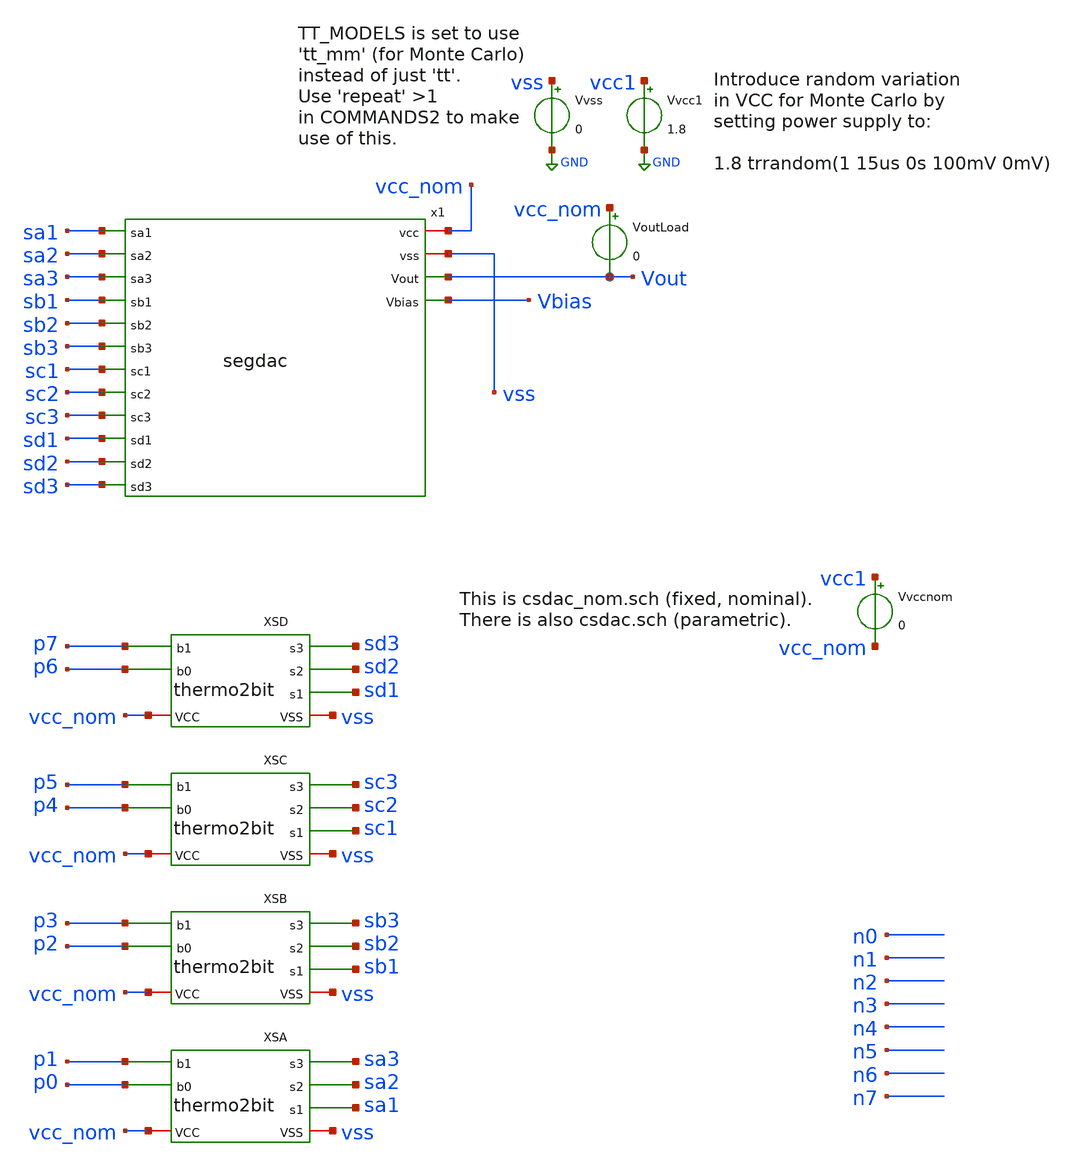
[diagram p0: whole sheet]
** sch_path: xschem/tb_segdac.sch
**.subckt tb_segdac
Vvcc1 vcc1 GND 1.8
Vvss vss GND 0
Vvccnom vcc1 vcc_nom 0
x1 sa1 vcc_nom sa2 vss sa3 Vout sb1 sb2 Vbias sb3 sc1 sc2 sc3 sd1 sd2 sd3 segdac
VoutLoad vcc_nom Vout 0
XSA vcc_nom vss sa3 p1 sa2 sa1 p0 thermo2bit
XSB vcc_nom vss sb3 p3 sb2 sb1 p2 thermo2bit
XSC vcc_nom vss sc3 p5 sc2 sc1 p4 thermo2bit
XSD vcc_nom vss sd3 p7 sd2 sd1 p6 thermo2bit
**** begin user architecture code




.param singlebits=0
.IF (singlebits == 1)
* Mode to just test each binary-weighted level:
Vxp0 p0 GND pulse 0v 1.8v 1u 1n 1n 1u 10u
Vxp1 p1 GND pulse 0v 1.8v 2u 1n 1n 1u 10u
Vxp2 p2 GND pulse 0v 1.8v 3u 1n 1n 1u 10u
Vxp3 p3 GND pulse 0v 1.8v 4u 1n 1n 1u 10u
Vxp4 p4 GND pulse 0v 1.8v 5u 1n 1n 1u 10u
Vxp5 p5 GND pulse 0v 1.8v 6u 1n 1n 1u 10u
Vxp6 p6 GND pulse 0v 1.8v 7u 1n 1n 1u 10u
Vxp7 p7 GND pulse 0v 1.8v 8u 1n 1n 1u 10u
Vxn0 n0 GND pulse 1.8v 0v 1u 1n 1n 1u 10u
Vxn1 n1 GND pulse 1.8v 0v 2u 1n 1n 1u 10u
Vxn2 n2 GND pulse 1.8v 0v 3u 1n 1n 1u 10u
Vxn3 n3 GND pulse 1.8v 0v 4u 1n 1n 1u 10u
Vxn4 n4 GND pulse 1.8v 0v 5u 1n 1n 1u 10u
Vxn5 n5 GND pulse 1.8v 0v 6u 1n 1n 1u 10u
Vxn6 n6 GND pulse 1.8v 0v 7u 1n 1n 1u 10u
Vxn7 n7 GND pulse 1.8v 0v 8u 1n 1n 1u 10u
.ELSEIF (singlebits == 0)
* Mode to test full 0..255 trange:
Vxp0 p0 GND pulse 1.8v 0v 0n 1n 1n 39n 80n
Vxp1 p1 GND pulse 1.8v 0v 0n 1n 1n 79n 160n
Vxp2 p2 GND pulse 1.8v 0v 0n 1n 1n 159n 320n
Vxp3 p3 GND pulse 1.8v 0v 0n 1n 1n 319n 640n
Vxp4 p4 GND pulse 1.8v 0v 0n 1n 1n 639n 1280n
Vxp5 p5 GND pulse 1.8v 0v 0n 1n 1n 1279n 2560n
Vxp6 p6 GND pulse 1.8v 0v 0n 1n 1n 2559n 5120n
Vxp7 p7 GND pulse 1.8v 0v 0n 1n 1n 5119n 10240n
Vxn0 n0 GND pulse 0v 1.8v 0n 1n 1n 39n 80n
Vxn1 n1 GND pulse 0v 1.8v 0n 1n 1n 79n 160n
Vxn2 n2 GND pulse 0v 1.8v 0n 1n 1n 159n 320n
Vxn3 n3 GND pulse 0v 1.8v 0n 1n 1n 319n 640n
Vxn4 n4 GND pulse 0v 1.8v 0n 1n 1n 639n 1280n
Vxn5 n5 GND pulse 0v 1.8v 0n 1n 1n 1279n 2560n
Vxn6 n6 GND pulse 0v 1.8v 0n 1n 1n 2559n 5120n
Vxn7 n7 GND pulse 0v 1.8v 0n 1n 1n 5119n 10240n
.ENDIF

.options savecurrents
.control

  * If using Monte Carlo, change to repeat to (say) 5:
  repeat 1
    save all
    tran 1n 12.8u
    write tb_segdac.raw i(vvss) vcc1 vbias vout i(vvccnom) i(voutload)
    + p0 p1 p2 p3 p4 p5 p6 p7
    + sa1 sa2 sa3 sb1 sb2 sb3 sc1 sc2 sc3 sd1 sd2 sd3
    set appendwrite
    reset
  end

*  save all
*  *reset
*  *alterparam MPW=4
*  *alterparam MMW=4
*  tran 1n 12.8u
*  write 11.raw i(vvcc) i(vvss) vpos vneg vbias

*  set appendwrite
*  alterparam MPW=4
*  alterparam MMW=4
*  reset
*  tran 1n 12.8u
*  write 11.raw i(vvcc) i(vvss) vpos vneg vbias

.endc




.lib $::SKYWATER_MODELS/sky130.lib.spice tt
.include $::SKYWATER_STDCELLS/sky130_fd_sc_hd.spice

**** end user architecture code
**.ends

* expanding   symbol:  segdac.sym # of pins=16
** sym_path: xschem/segdac.sym
** sch_path: xschem/segdac.sch
.subckt segdac sa1 vcc sa2 vss sa3 Vout sb1 sb2 Vbias sb3 sc1 sc2 sc3 sd1 sd2 sd3
*.iopin vcc
*.iopin vss
*.opin Vout
*.opin Vbias
*.ipin sa1
*.ipin sa2
*.ipin sa3
*.ipin sb1
*.ipin sb2
*.ipin sb3
*.ipin sc1
*.ipin sc2
*.ipin sc3
*.ipin sd1
*.ipin sd2
*.ipin sd3
XMprog Vbias vss vcc vcc sky130_fd_pr__pfet_01v8 L=0.6 W=0.5 nf=1 ad='int((nf+1)/2) * W/nf * 0.29' as='int((nf+2)/2) * W/nf * 0.29'
+ pd='2*int((nf+1)/2) * (W/nf + 0.29)' ps='2*int((nf+2)/2) * (W/nf + 0.29)' nrd='0.29 / W' nrs='0.29 / W'
+ sa=0 sb=0 sd=0 mult=1 m=1
XMmirror Vbias Vbias vss vss sky130_fd_pr__nfet_01v8 L=0.15 W=1 nf=1 ad='int((nf+1)/2) * W/nf * 0.29'
+ as='int((nf+2)/2) * W/nf * 0.29' pd='2*int((nf+1)/2) * (W/nf + 0.29)' ps='2*int((nf+2)/2) * (W/nf + 0.29)'
+ nrd='0.29 / W' nrs='0.29 / W' sa=0 sb=0 sd=0 mult=1 m=1
XMia1 net1 Vbias vss vss sky130_fd_pr__nfet_01v8 L=2.4 W=0.5 nf=1 ad='int((nf+1)/2) * W/nf * 0.29' as='int((nf+2)/2) * W/nf * 0.29'
+ pd='2*int((nf+1)/2) * (W/nf + 0.29)' ps='2*int((nf+2)/2) * (W/nf + 0.29)' nrd='0.29 / W' nrs='0.29 / W'
+ sa=0 sb=0 sd=0 mult=1 m=1
XMia2 net2 Vbias vss vss sky130_fd_pr__nfet_01v8 L=2.4 W=0.5 nf=1 ad='int((nf+1)/2) * W/nf * 0.29' as='int((nf+2)/2) * W/nf * 0.29'
+ pd='2*int((nf+1)/2) * (W/nf + 0.29)' ps='2*int((nf+2)/2) * (W/nf + 0.29)' nrd='0.29 / W' nrs='0.29 / W'
+ sa=0 sb=0 sd=0 mult=1 m=1
XMia3 net3 Vbias vss vss sky130_fd_pr__nfet_01v8 L=2.4 W=0.5 nf=1 ad='int((nf+1)/2) * W/nf * 0.29' as='int((nf+2)/2) * W/nf * 0.29'
+ pd='2*int((nf+1)/2) * (W/nf + 0.29)' ps='2*int((nf+2)/2) * (W/nf + 0.29)' nrd='0.29 / W' nrs='0.29 / W'
+ sa=0 sb=0 sd=0 mult=1 m=1
XMsa1 Vout sa1 net1 vss sky130_fd_pr__nfet_01v8 L=0.15 W=0.5 nf=1 ad='int((nf+1)/2) * W/nf * 0.29' as='int((nf+2)/2) * W/nf * 0.29'
+ pd='2*int((nf+1)/2) * (W/nf + 0.29)' ps='2*int((nf+2)/2) * (W/nf + 0.29)' nrd='0.29 / W' nrs='0.29 / W'
+ sa=0 sb=0 sd=0 mult=1 m=1
XMsa2 Vout sa2 net2 vss sky130_fd_pr__nfet_01v8 L=0.15 W=0.5 nf=1 ad='int((nf+1)/2) * W/nf * 0.29' as='int((nf+2)/2) * W/nf * 0.29'
+ pd='2*int((nf+1)/2) * (W/nf + 0.29)' ps='2*int((nf+2)/2) * (W/nf + 0.29)' nrd='0.29 / W' nrs='0.29 / W'
+ sa=0 sb=0 sd=0 mult=1 m=1
XMsa3 Vout sa3 net3 vss sky130_fd_pr__nfet_01v8 L=0.15 W=0.5 nf=1 ad='int((nf+1)/2) * W/nf * 0.29' as='int((nf+2)/2) * W/nf * 0.29'
+ pd='2*int((nf+1)/2) * (W/nf + 0.29)' ps='2*int((nf+2)/2) * (W/nf + 0.29)' nrd='0.29 / W' nrs='0.29 / W'
+ sa=0 sb=0 sd=0 mult=1 m=1
XMib1 net4 Vbias vss vss sky130_fd_pr__nfet_01v8 L=1.2 W=1.1 nf=1 ad='int((nf+1)/2) * W/nf * 0.29' as='int((nf+2)/2) * W/nf * 0.29'
+ pd='2*int((nf+1)/2) * (W/nf + 0.29)' ps='2*int((nf+2)/2) * (W/nf + 0.29)' nrd='0.29 / W' nrs='0.29 / W'
+ sa=0 sb=0 sd=0 mult=1 m=1
XMib2 net5 Vbias vss vss sky130_fd_pr__nfet_01v8 L=1.2 W=1.1 nf=1 ad='int((nf+1)/2) * W/nf * 0.29' as='int((nf+2)/2) * W/nf * 0.29'
+ pd='2*int((nf+1)/2) * (W/nf + 0.29)' ps='2*int((nf+2)/2) * (W/nf + 0.29)' nrd='0.29 / W' nrs='0.29 / W'
+ sa=0 sb=0 sd=0 mult=1 m=1
XMib3 net6 Vbias vss vss sky130_fd_pr__nfet_01v8 L=1.2 W=1.1 nf=1 ad='int((nf+1)/2) * W/nf * 0.29' as='int((nf+2)/2) * W/nf * 0.29'
+ pd='2*int((nf+1)/2) * (W/nf + 0.29)' ps='2*int((nf+2)/2) * (W/nf + 0.29)' nrd='0.29 / W' nrs='0.29 / W'
+ sa=0 sb=0 sd=0 mult=1 m=1
XMsb1 Vout sb1 net4 vss sky130_fd_pr__nfet_01v8 L=0.15 W=0.5 nf=1 ad='int((nf+1)/2) * W/nf * 0.29' as='int((nf+2)/2) * W/nf * 0.29'
+ pd='2*int((nf+1)/2) * (W/nf + 0.29)' ps='2*int((nf+2)/2) * (W/nf + 0.29)' nrd='0.29 / W' nrs='0.29 / W'
+ sa=0 sb=0 sd=0 mult=1 m=1
XMsb2 Vout sb2 net5 vss sky130_fd_pr__nfet_01v8 L=0.15 W=0.5 nf=1 ad='int((nf+1)/2) * W/nf * 0.29' as='int((nf+2)/2) * W/nf * 0.29'
+ pd='2*int((nf+1)/2) * (W/nf + 0.29)' ps='2*int((nf+2)/2) * (W/nf + 0.29)' nrd='0.29 / W' nrs='0.29 / W'
+ sa=0 sb=0 sd=0 mult=1 m=1
XMsb3 Vout sb3 net6 vss sky130_fd_pr__nfet_01v8 L=0.15 W=0.5 nf=1 ad='int((nf+1)/2) * W/nf * 0.29' as='int((nf+2)/2) * W/nf * 0.29'
+ pd='2*int((nf+1)/2) * (W/nf + 0.29)' ps='2*int((nf+2)/2) * (W/nf + 0.29)' nrd='0.29 / W' nrs='0.29 / W'
+ sa=0 sb=0 sd=0 mult=1 m=1
XMic1 net7 Vbias vss vss sky130_fd_pr__nfet_01v8 L=0.25 W=1.8 nf=1 ad='int((nf+1)/2) * W/nf * 0.29' as='int((nf+2)/2) * W/nf * 0.29'
+ pd='2*int((nf+1)/2) * (W/nf + 0.29)' ps='2*int((nf+2)/2) * (W/nf + 0.29)' nrd='0.29 / W' nrs='0.29 / W'
+ sa=0 sb=0 sd=0 mult=1 m=1
XMic2 net8 Vbias vss vss sky130_fd_pr__nfet_01v8 L=0.25 W=1.8 nf=1 ad='int((nf+1)/2) * W/nf * 0.29' as='int((nf+2)/2) * W/nf * 0.29'
+ pd='2*int((nf+1)/2) * (W/nf + 0.29)' ps='2*int((nf+2)/2) * (W/nf + 0.29)' nrd='0.29 / W' nrs='0.29 / W'
+ sa=0 sb=0 sd=0 mult=1 m=1
XMic3 net9 Vbias vss vss sky130_fd_pr__nfet_01v8 L=0.25 W=1.8 nf=1 ad='int((nf+1)/2) * W/nf * 0.29' as='int((nf+2)/2) * W/nf * 0.29'
+ pd='2*int((nf+1)/2) * (W/nf + 0.29)' ps='2*int((nf+2)/2) * (W/nf + 0.29)' nrd='0.29 / W' nrs='0.29 / W'
+ sa=0 sb=0 sd=0 mult=1 m=1
XMsc1 Vout sc1 net7 vss sky130_fd_pr__nfet_01v8 L=0.15 W=1.9 nf=1 ad='int((nf+1)/2) * W/nf * 0.29' as='int((nf+2)/2) * W/nf * 0.29'
+ pd='2*int((nf+1)/2) * (W/nf + 0.29)' ps='2*int((nf+2)/2) * (W/nf + 0.29)' nrd='0.29 / W' nrs='0.29 / W'
+ sa=0 sb=0 sd=0 mult=1 m=1
XMsc2 Vout sc2 net8 vss sky130_fd_pr__nfet_01v8 L=0.15 W=1.9 nf=1 ad='int((nf+1)/2) * W/nf * 0.29' as='int((nf+2)/2) * W/nf * 0.29'
+ pd='2*int((nf+1)/2) * (W/nf + 0.29)' ps='2*int((nf+2)/2) * (W/nf + 0.29)' nrd='0.29 / W' nrs='0.29 / W'
+ sa=0 sb=0 sd=0 mult=1 m=1
XMsc3 Vout sc3 net9 vss sky130_fd_pr__nfet_01v8 L=0.15 W=1.9 nf=1 ad='int((nf+1)/2) * W/nf * 0.29' as='int((nf+2)/2) * W/nf * 0.29'
+ pd='2*int((nf+1)/2) * (W/nf + 0.29)' ps='2*int((nf+2)/2) * (W/nf + 0.29)' nrd='0.29 / W' nrs='0.29 / W'
+ sa=0 sb=0 sd=0 mult=1 m=1
XMid1 net10 Vbias vss vss sky130_fd_pr__nfet_01v8 L=0.15 W=4 nf=1 ad='int((nf+1)/2) * W/nf * 0.29' as='int((nf+2)/2) * W/nf * 0.29'
+ pd='2*int((nf+1)/2) * (W/nf + 0.29)' ps='2*int((nf+2)/2) * (W/nf + 0.29)' nrd='0.29 / W' nrs='0.29 / W'
+ sa=0 sb=0 sd=0 mult=1 m=1
XMid2 net11 Vbias vss vss sky130_fd_pr__nfet_01v8 L=0.15 W=4 nf=1 ad='int((nf+1)/2) * W/nf * 0.29' as='int((nf+2)/2) * W/nf * 0.29'
+ pd='2*int((nf+1)/2) * (W/nf + 0.29)' ps='2*int((nf+2)/2) * (W/nf + 0.29)' nrd='0.29 / W' nrs='0.29 / W'
+ sa=0 sb=0 sd=0 mult=1 m=1
XMid3 net12 Vbias vss vss sky130_fd_pr__nfet_01v8 L=0.15 W=4 nf=1 ad='int((nf+1)/2) * W/nf * 0.29' as='int((nf+2)/2) * W/nf * 0.29'
+ pd='2*int((nf+1)/2) * (W/nf + 0.29)' ps='2*int((nf+2)/2) * (W/nf + 0.29)' nrd='0.29 / W' nrs='0.29 / W'
+ sa=0 sb=0 sd=0 mult=1 m=1
XMsd1 Vout sd1 net10 vss sky130_fd_pr__nfet_01v8 L=0.15 W=5.7 nf=1 ad='int((nf+1)/2) * W/nf * 0.29' as='int((nf+2)/2) * W/nf * 0.29'
+ pd='2*int((nf+1)/2) * (W/nf + 0.29)' ps='2*int((nf+2)/2) * (W/nf + 0.29)' nrd='0.29 / W' nrs='0.29 / W'
+ sa=0 sb=0 sd=0 mult=1 m=1
XMsd2 Vout sd2 net11 vss sky130_fd_pr__nfet_01v8 L=0.15 W=5.7 nf=1 ad='int((nf+1)/2) * W/nf * 0.29' as='int((nf+2)/2) * W/nf * 0.29'
+ pd='2*int((nf+1)/2) * (W/nf + 0.29)' ps='2*int((nf+2)/2) * (W/nf + 0.29)' nrd='0.29 / W' nrs='0.29 / W'
+ sa=0 sb=0 sd=0 mult=1 m=1
XMsd3 Vout sd3 net12 vss sky130_fd_pr__nfet_01v8 L=0.15 W=5.7 nf=1 ad='int((nf+1)/2) * W/nf * 0.29' as='int((nf+2)/2) * W/nf * 0.29'
+ pd='2*int((nf+1)/2) * (W/nf + 0.29)' ps='2*int((nf+2)/2) * (W/nf + 0.29)' nrd='0.29 / W' nrs='0.29 / W'
+ sa=0 sb=0 sd=0 mult=1 m=1
.ends


* expanding   symbol:  thermo2bit.sym # of pins=7
** sym_path: xschem/thermo2bit.sym
** sch_path: xschem/thermo2bit.sch
.subckt thermo2bit VCC VSS s3 b1 s2 s1 b0
*.ipin b1
*.opin s2
*.ipin b0
*.opin s1
*.opin s3
*.iopin VCC
*.iopin VSS
x2 b0 b1 VSS VSS VCC VCC s3 sky130_fd_sc_hd__and2_1
x3 b1 b0 VSS VSS VCC VCC s1 sky130_fd_sc_hd__or2_1
R1 s2 b1 0 m=1
.ends

.GLOBAL GND
.end
